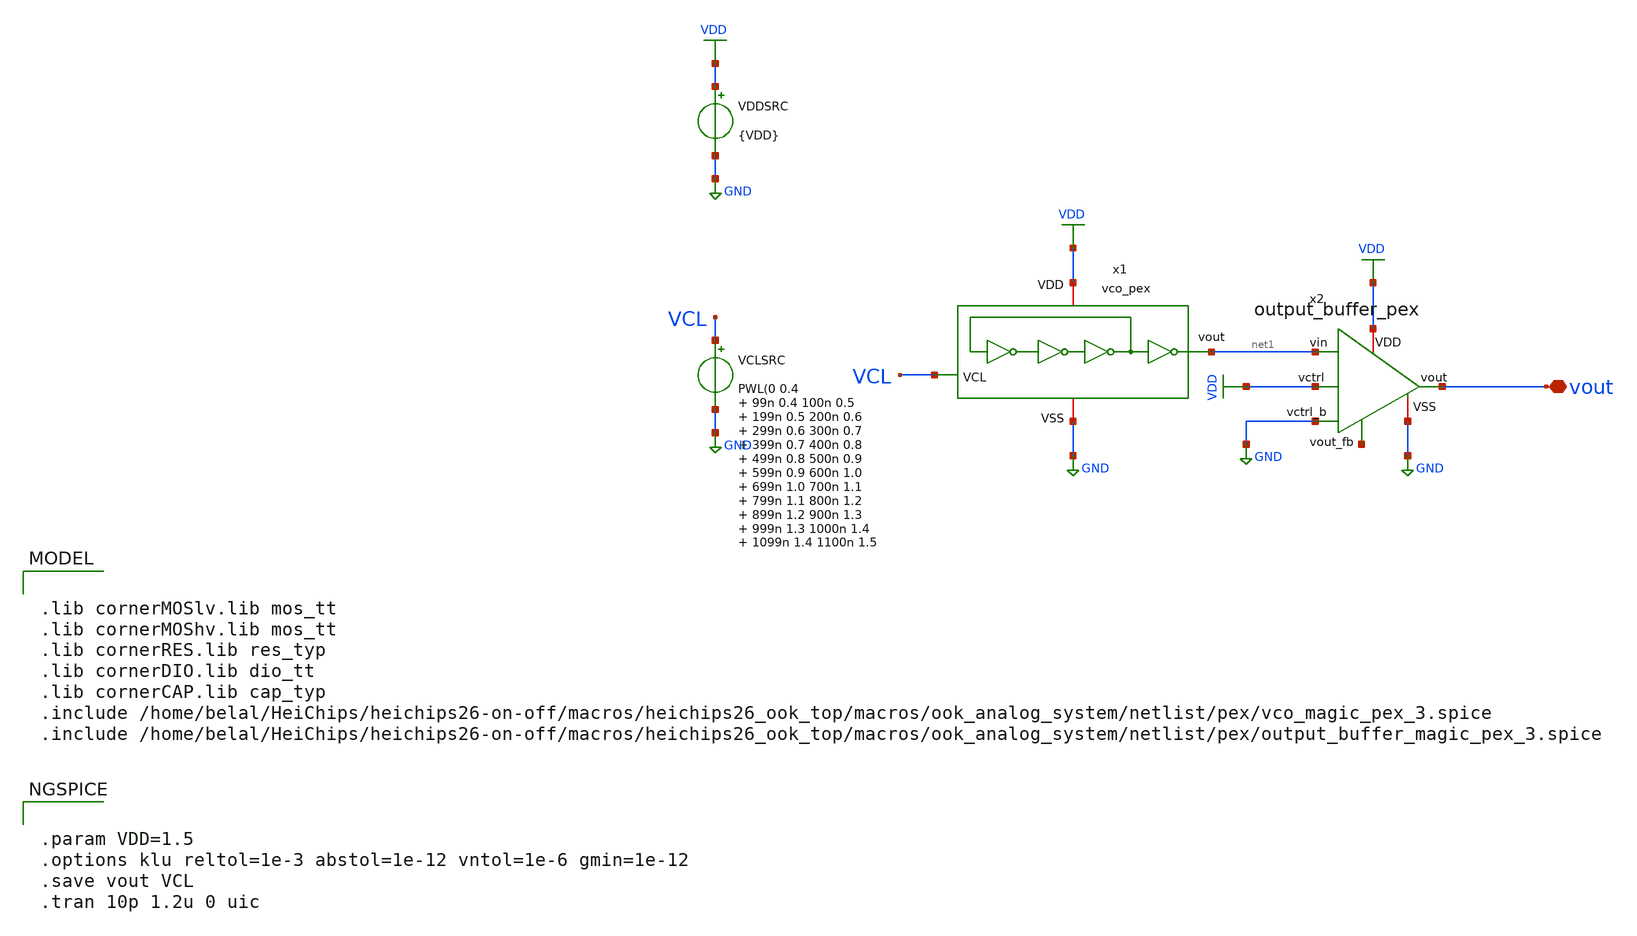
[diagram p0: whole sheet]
** sch_path: macros/heichips26_ook_top/macros/ook_analog_system/testbenches/xschem/vco_tb_tran.sch
**.subckt vco_tb_tran vout
*.iopin vout
x1 net1 VDD GND VCL vco_pex
VDDSRC VDD GND {VDD}
VCLSRC VCL GND PWL(0 0.4 99n 0.4 100n 0.5 199n 0.5 200n 0.6 299n 0.6 300n 0.7 399n 0.7 400n 0.8 499n
+ 0.8 500n 0.9 599n 0.9 600n 1.0 699n 1.0 700n 1.1 799n 1.1 800n 1.2 899n 1.2 900n 1.3 999n 1.3 1000n 1.4
+ 1099n 1.4 1100n 1.5 1200n 1.5)
x2 net2 VDD VDD net1 vout GND GND output_buffer_pex
**** begin user architecture code


.param VDD=1.5
.options klu reltol=1e-3 abstol=1e-12 vntol=1e-6 gmin=1e-12
.save vout VCL
.tran 10p 1.2u 0 uic



.lib cornerMOSlv.lib mos_tt
.lib cornerMOShv.lib mos_tt
.lib cornerRES.lib res_typ
.lib cornerDIO.lib dio_tt
.lib cornerCAP.lib cap_typ
.include /home/belal/HeiChips/heichips26-on-off/macros/heichips26_ook_top/macros/ook_analog_system/netlist/pex/vco_magic_pex_3.spice
.include /home/belal/HeiChips/heichips26-on-off/macros/heichips26_ook_top/macros/ook_analog_system/netlist/pex/output_buffer_magic_pex_3.spice


**** end user architecture code
**.ends
.GLOBAL VDD
.GLOBAL GND
.end
